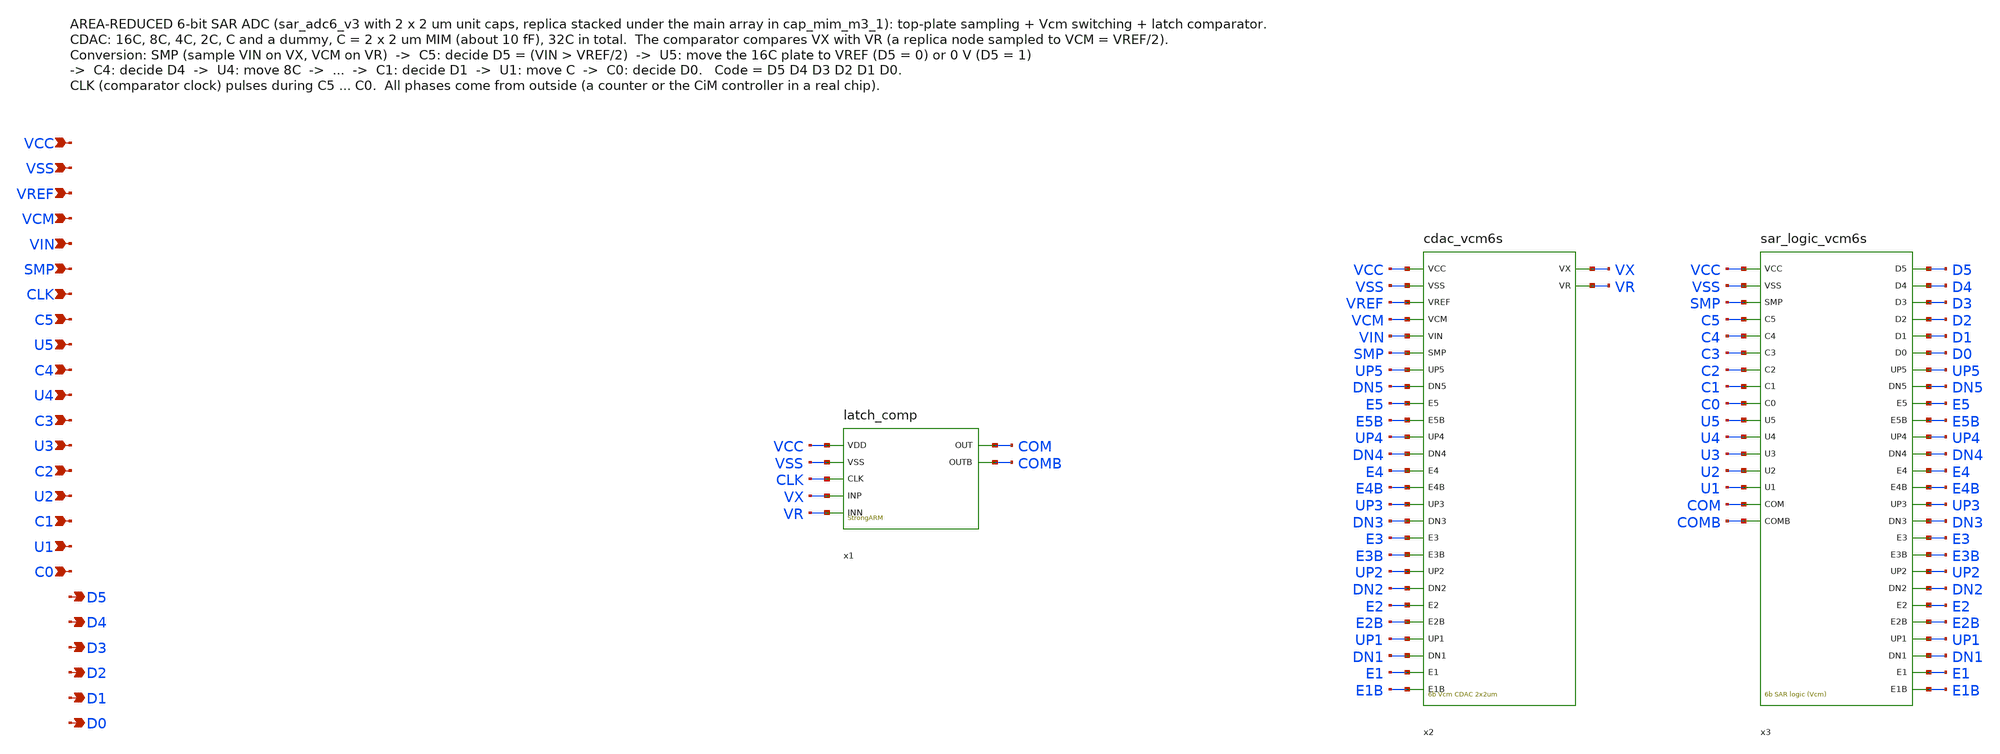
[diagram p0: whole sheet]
** sch_path: SAR_improved/sar_adc6_v3s.sch
**.subckt sar_adc6_v3s VCC VSS VREF VCM VIN SMP CLK C5 U5 C4 U4 C3 U3 C2 U2 C1 U1 C0 D5 D4 D3 D2 D1
*+ D0
*.ipin VCC
*.ipin VSS
*.ipin VREF
*.ipin VCM
*.ipin VIN
*.ipin SMP
*.ipin CLK
*.ipin C5
*.ipin U5
*.ipin C4
*.ipin U4
*.ipin C3
*.ipin U3
*.ipin C2
*.ipin U2
*.ipin C1
*.ipin U1
*.ipin C0
*.opin D5
*.opin D4
*.opin D3
*.opin D2
*.opin D1
*.opin D0
x1 VCC VSS CLK VX VR COM COMB latch_comp
x2 VCC VSS VREF VCM VIN SMP UP5 DN5 E5 E5B UP4 DN4 E4 E4B UP3 DN3 E3 E3B UP2 DN2 E2 E2B UP1 DN1 E1
+ E1B VX VR cdac_vcm6s
x3 VCC VSS SMP C5 C4 C3 C2 C1 C0 U5 U4 U3 U2 U1 COM COMB D5 D4 D3 D2 D1 D0 UP5 DN5 E5 E5B UP4 DN4 E4
+ E4B UP3 DN3 E3 E3B UP2 DN2 E2 E2B UP1 DN1 E1 E1B sar_logic_vcm6s
**.ends
.end
